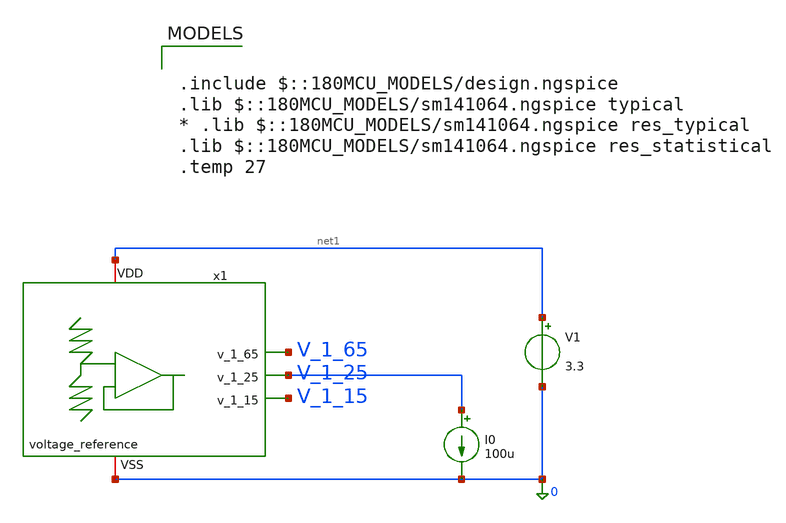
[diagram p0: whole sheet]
** sch_path: lvs/schematics/tb_voltage_reference.sch
**.subckt tb_voltage_reference
V1 net1 0 3.3
I0 V_1_25 0 100u
x1 net1 V_1_65 V_1_25 V_1_15 0 voltage_reference
**** begin user architecture code

.include $::180MCU_MODELS/design.ngspice
.lib $::180MCU_MODELS/sm141064.ngspice typical
* .lib $::180MCU_MODELS/sm141064.ngspice res_typical
.lib $::180MCU_MODELS/sm141064.ngspice res_statistical
.temp 27



.control
  op
  print all
  print @m.x1.xm2.m0[vgs] @m.x1.xm3.m0[vgs]
  print @m.x1.xm7.m0[vgs] @m.x1.xm8.m0[vgs]
  print @m.x1.xm12.m0[vgs] @m.x1.xm13.m0[vgs]
  print v(V_1_65) v(V_1_25) v(V_1_15)
.endc


**** end user architecture code
**.ends
.end
